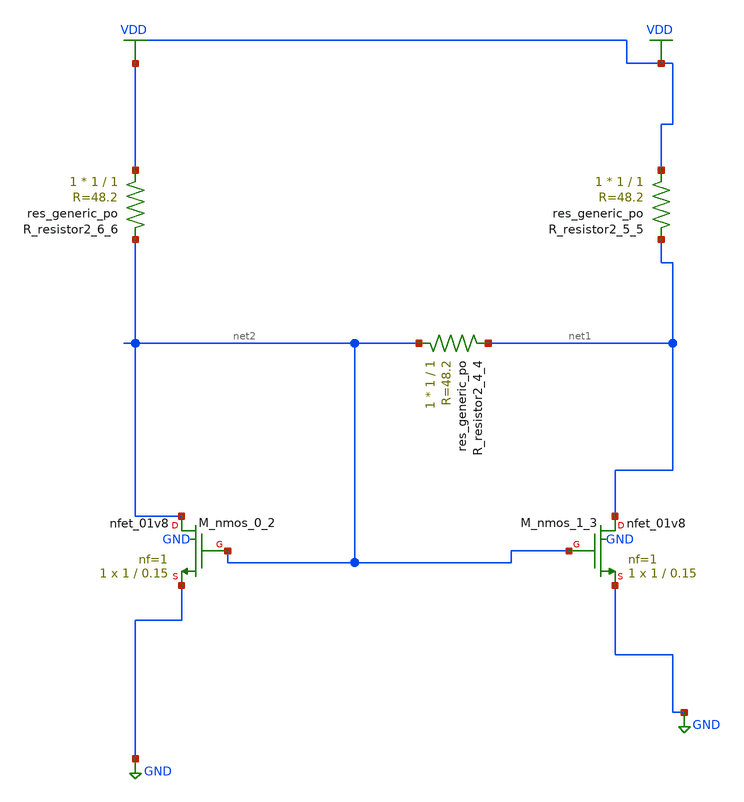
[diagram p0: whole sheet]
** sch_path: schematics/AMSNet/322.sch
**.subckt 322
XM_nmos_0_2 net2 net2 GND GND sky130_fd_pr__nfet_01v8 L=0.15 W=1 nf=1 ad='int((1 + 1)/2) * 1 / 1 * 0.29'
+ as='int((1 + 2)/2) * 1 / 1 * 0.29' pd='2*int((1 + 1)/2) * (1 / 1 + 0.29)' ps='2*int((1 + 2)/2) * (1 / 1 + 0.29)'
+ nrd='0.29 / 1 ' nrs='0.29 / 1 ' sa=0 sb=0 sd=0 mult=1 m=1
XM_nmos_1_3 net1 net2 GND GND sky130_fd_pr__nfet_01v8 L=0.15 W=1 nf=1 ad='int((1 + 1)/2) * 1 / 1 * 0.29'
+ as='int((1 + 2)/2) * 1 / 1 * 0.29' pd='2*int((1 + 1)/2) * (1 / 1 + 0.29)' ps='2*int((1 + 2)/2) * (1 / 1 + 0.29)'
+ nrd='0.29 / 1 ' nrs='0.29 / 1 ' sa=0 sb=0 sd=0 mult=1 m=1
XR_resistor2_4_4 net2 net1 sky130_fd_pr__res_generic_po W=1 L=1 m=1
XR_resistor2_5_5 VDD net1 sky130_fd_pr__res_generic_po W=1 L=1 m=1
XR_resistor2_6_6 VDD net2 sky130_fd_pr__res_generic_po W=1 L=1 m=1
**.ends
.GLOBAL GND
.GLOBAL VDD
.end
